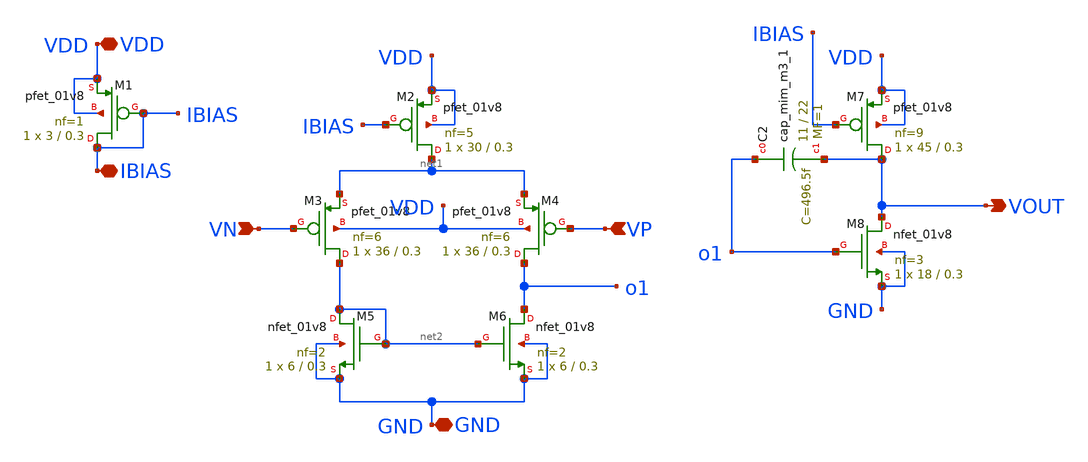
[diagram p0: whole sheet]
** sch_path: Fractional Order PID/OPAMP/opamp.sch
**.subckt opamp VDD IBIAS VN VP GND VOUT
*.iopin VDD
*.iopin IBIAS
*.ipin VN
*.ipin VP
*.iopin GND
*.opin VOUT
XM1 IBIAS IBIAS VDD VDD sky130_fd_pr__pfet_01v8 L=0.3 W=3 nf=1 ad='int((nf+1)/2) * W/nf * 0.29' as='int((nf+2)/2) * W/nf * 0.29'
+ pd='2*int((nf+1)/2) * (W/nf + 0.29)' ps='2*int((nf+2)/2) * (W/nf + 0.29)' nrd='0.29 / W' nrs='0.29 / W'
+ sa=0 sb=0 sd=0 mult=1 m=1
XM2 net1 IBIAS VDD VDD sky130_fd_pr__pfet_01v8 L=0.3 W=30 nf=5 ad='int((nf+1)/2) * W/nf * 0.29' as='int((nf+2)/2) * W/nf * 0.29'
+ pd='2*int((nf+1)/2) * (W/nf + 0.29)' ps='2*int((nf+2)/2) * (W/nf + 0.29)' nrd='0.29 / W' nrs='0.29 / W'
+ sa=0 sb=0 sd=0 mult=1 m=1
XM3 net2 VN net1 VDD sky130_fd_pr__pfet_01v8 L=0.3 W=36 nf=6 ad='int((nf+1)/2) * W/nf * 0.29' as='int((nf+2)/2) * W/nf * 0.29'
+ pd='2*int((nf+1)/2) * (W/nf + 0.29)' ps='2*int((nf+2)/2) * (W/nf + 0.29)' nrd='0.29 / W' nrs='0.29 / W'
+ sa=0 sb=0 sd=0 mult=1 m=1
XM4 o1 VP net1 VDD sky130_fd_pr__pfet_01v8 L=0.3 W=36 nf=6 ad='int((nf+1)/2) * W/nf * 0.29' as='int((nf+2)/2) * W/nf * 0.29'
+ pd='2*int((nf+1)/2) * (W/nf + 0.29)' ps='2*int((nf+2)/2) * (W/nf + 0.29)' nrd='0.29 / W' nrs='0.29 / W'
+ sa=0 sb=0 sd=0 mult=1 m=1
XM5 net2 net2 GND GND sky130_fd_pr__nfet_01v8 L=0.3 W=6 nf=2 ad='int((nf+1)/2) * W/nf * 0.29' as='int((nf+2)/2) * W/nf * 0.29'
+ pd='2*int((nf+1)/2) * (W/nf + 0.29)' ps='2*int((nf+2)/2) * (W/nf + 0.29)' nrd='0.29 / W' nrs='0.29 / W'
+ sa=0 sb=0 sd=0 mult=1 m=1
XM6 o1 net2 GND GND sky130_fd_pr__nfet_01v8 L=0.3 W=6 nf=2 ad='int((nf+1)/2) * W/nf * 0.29' as='int((nf+2)/2) * W/nf * 0.29'
+ pd='2*int((nf+1)/2) * (W/nf + 0.29)' ps='2*int((nf+2)/2) * (W/nf + 0.29)' nrd='0.29 / W' nrs='0.29 / W'
+ sa=0 sb=0 sd=0 mult=1 m=1
XM7 VOUT IBIAS VDD VDD sky130_fd_pr__pfet_01v8 L=0.3 W=45 nf=9 ad='int((nf+1)/2) * W/nf * 0.29' as='int((nf+2)/2) * W/nf * 0.29'
+ pd='2*int((nf+1)/2) * (W/nf + 0.29)' ps='2*int((nf+2)/2) * (W/nf + 0.29)' nrd='0.29 / W' nrs='0.29 / W'
+ sa=0 sb=0 sd=0 mult=1 m=1
XM8 VOUT o1 GND GND sky130_fd_pr__nfet_01v8 L=0.3 W=18 nf=3 ad='int((nf+1)/2) * W/nf * 0.29' as='int((nf+2)/2) * W/nf * 0.29'
+ pd='2*int((nf+1)/2) * (W/nf + 0.29)' ps='2*int((nf+2)/2) * (W/nf + 0.29)' nrd='0.29 / W' nrs='0.29 / W'
+ sa=0 sb=0 sd=0 mult=1 m=1
XC2 o1 VOUT sky130_fd_pr__cap_mim_m3_1 W=11 L=22 MF=1 m=1
**.ends
.end
